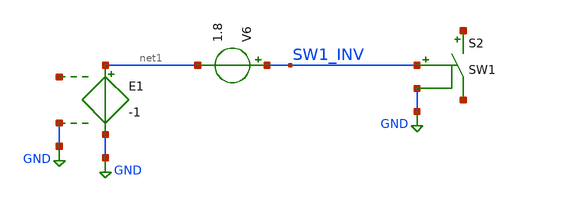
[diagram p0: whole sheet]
** sch_path: projects/ASU/EEE572/schematic/untitled.sch
**.subckt untitled
S2 net2 net3 SW1_INV GND SW1
E1 net1 GND net4 GND -1
V6 SW1_INV net1 1.8
**.ends
.GLOBAL GND
**** begin user architecture code
.MODEL SW1 SW( VT=0.9 VH=0.01 RON=0.01 ROFF=10G )
**** end user architecture code
.end
